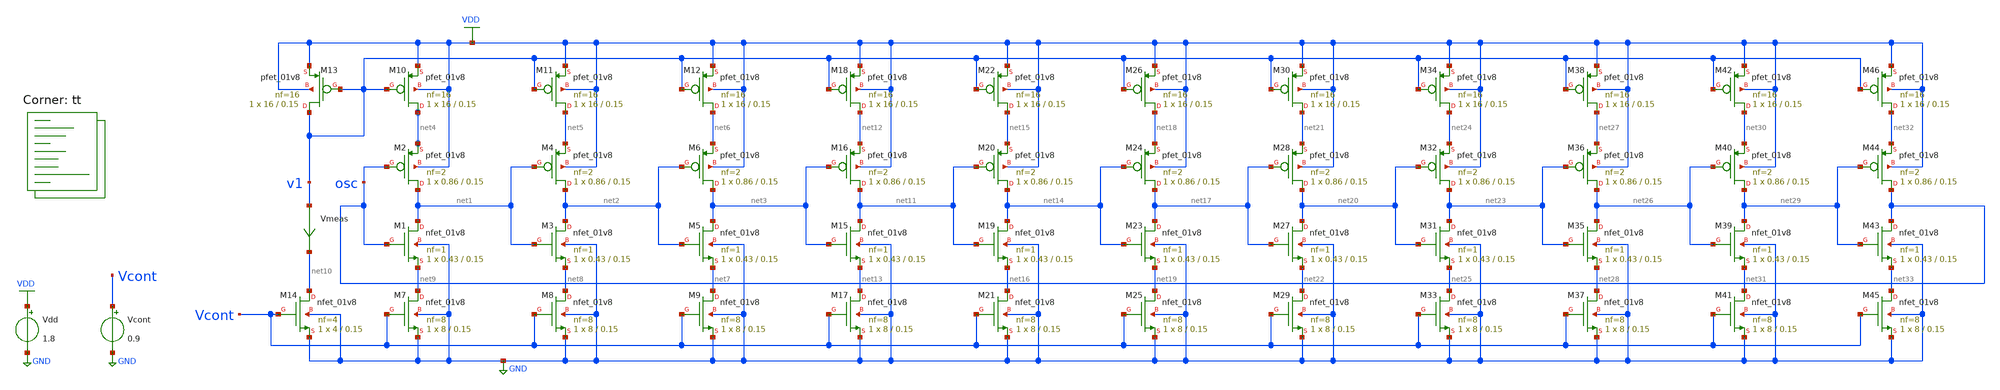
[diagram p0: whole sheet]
** sch_path: projects/pll/vco/xschem_ngspice/tb_current_starved_VCO7.sch
**.subckt tb_current_starved_VCO7
XM1 net1 osc net9 GND sky130_fd_pr__nfet_01v8 L=0.15 W=0.43 nf=1 ad='int((nf+1)/2) * W/nf * 0.29' as='int((nf+2)/2) * W/nf * 0.29'
+ pd='2*int((nf+1)/2) * (W/nf + 0.29)' ps='2*int((nf+2)/2) * (W/nf + 0.29)' nrd='0.29 / W' nrs='0.29 / W'
+ sa=0 sb=0 sd=0 mult=1 m=1
XM2 net1 osc net4 VDD sky130_fd_pr__pfet_01v8 L=0.15 W=0.86 nf=2 ad='int((nf+1)/2) * W/nf * 0.29' as='int((nf+2)/2) * W/nf * 0.29'
+ pd='2*int((nf+1)/2) * (W/nf + 0.29)' ps='2*int((nf+2)/2) * (W/nf + 0.29)' nrd='0.29 / W' nrs='0.29 / W'
+ sa=0 sb=0 sd=0 mult=1 m=1
XM3 net2 net1 net8 GND sky130_fd_pr__nfet_01v8 L=0.15 W=0.43 nf=1 ad='int((nf+1)/2) * W/nf * 0.29' as='int((nf+2)/2) * W/nf * 0.29'
+ pd='2*int((nf+1)/2) * (W/nf + 0.29)' ps='2*int((nf+2)/2) * (W/nf + 0.29)' nrd='0.29 / W' nrs='0.29 / W'
+ sa=0 sb=0 sd=0 mult=1 m=1
XM4 net2 net1 net5 VDD sky130_fd_pr__pfet_01v8 L=0.15 W=0.86 nf=2 ad='int((nf+1)/2) * W/nf * 0.29' as='int((nf+2)/2) * W/nf * 0.29'
+ pd='2*int((nf+1)/2) * (W/nf + 0.29)' ps='2*int((nf+2)/2) * (W/nf + 0.29)' nrd='0.29 / W' nrs='0.29 / W'
+ sa=0 sb=0 sd=0 mult=1 m=1
XM5 net3 net2 net7 GND sky130_fd_pr__nfet_01v8 L=0.15 W=0.43 nf=1 ad='int((nf+1)/2) * W/nf * 0.29' as='int((nf+2)/2) * W/nf * 0.29'
+ pd='2*int((nf+1)/2) * (W/nf + 0.29)' ps='2*int((nf+2)/2) * (W/nf + 0.29)' nrd='0.29 / W' nrs='0.29 / W'
+ sa=0 sb=0 sd=0 mult=1 m=1
XM6 net3 net2 net6 VDD sky130_fd_pr__pfet_01v8 L=0.15 W=0.86 nf=2 ad='int((nf+1)/2) * W/nf * 0.29' as='int((nf+2)/2) * W/nf * 0.29'
+ pd='2*int((nf+1)/2) * (W/nf + 0.29)' ps='2*int((nf+2)/2) * (W/nf + 0.29)' nrd='0.29 / W' nrs='0.29 / W'
+ sa=0 sb=0 sd=0 mult=1 m=1
XM7 net9 Vcont GND GND sky130_fd_pr__nfet_01v8 L=0.15 W=8 nf=8 ad='int((nf+1)/2) * W/nf * 0.29' as='int((nf+2)/2) * W/nf * 0.29'
+ pd='2*int((nf+1)/2) * (W/nf + 0.29)' ps='2*int((nf+2)/2) * (W/nf + 0.29)' nrd='0.29 / W' nrs='0.29 / W'
+ sa=0 sb=0 sd=0 mult=1 m=1
XM8 net8 Vcont GND GND sky130_fd_pr__nfet_01v8 L=0.15 W=8 nf=8 ad='int((nf+1)/2) * W/nf * 0.29' as='int((nf+2)/2) * W/nf * 0.29'
+ pd='2*int((nf+1)/2) * (W/nf + 0.29)' ps='2*int((nf+2)/2) * (W/nf + 0.29)' nrd='0.29 / W' nrs='0.29 / W'
+ sa=0 sb=0 sd=0 mult=1 m=1
XM9 net7 Vcont GND GND sky130_fd_pr__nfet_01v8 L=0.15 W=8 nf=8 ad='int((nf+1)/2) * W/nf * 0.29' as='int((nf+2)/2) * W/nf * 0.29'
+ pd='2*int((nf+1)/2) * (W/nf + 0.29)' ps='2*int((nf+2)/2) * (W/nf + 0.29)' nrd='0.29 / W' nrs='0.29 / W'
+ sa=0 sb=0 sd=0 mult=1 m=1
XM10 net4 v1 VDD VDD sky130_fd_pr__pfet_01v8 L=0.15 W=16 nf=16 ad='int((nf+1)/2) * W/nf * 0.29' as='int((nf+2)/2) * W/nf * 0.29'
+ pd='2*int((nf+1)/2) * (W/nf + 0.29)' ps='2*int((nf+2)/2) * (W/nf + 0.29)' nrd='0.29 / W' nrs='0.29 / W'
+ sa=0 sb=0 sd=0 mult=1 m=1
XM11 net5 v1 VDD VDD sky130_fd_pr__pfet_01v8 L=0.15 W=16 nf=16 ad='int((nf+1)/2) * W/nf * 0.29' as='int((nf+2)/2) * W/nf * 0.29'
+ pd='2*int((nf+1)/2) * (W/nf + 0.29)' ps='2*int((nf+2)/2) * (W/nf + 0.29)' nrd='0.29 / W' nrs='0.29 / W'
+ sa=0 sb=0 sd=0 mult=1 m=1
XM12 net6 v1 VDD VDD sky130_fd_pr__pfet_01v8 L=0.15 W=16 nf=16 ad='int((nf+1)/2) * W/nf * 0.29' as='int((nf+2)/2) * W/nf * 0.29'
+ pd='2*int((nf+1)/2) * (W/nf + 0.29)' ps='2*int((nf+2)/2) * (W/nf + 0.29)' nrd='0.29 / W' nrs='0.29 / W'
+ sa=0 sb=0 sd=0 mult=1 m=1
Vdd VDD GND 1.8
Vcont Vcont GND 0.9
XM13 v1 v1 VDD VDD sky130_fd_pr__pfet_01v8 L=0.15 W=16 nf=16 ad='int((nf+1)/2) * W/nf * 0.29' as='int((nf+2)/2) * W/nf * 0.29'
+ pd='2*int((nf+1)/2) * (W/nf + 0.29)' ps='2*int((nf+2)/2) * (W/nf + 0.29)' nrd='0.29 / W' nrs='0.29 / W'
+ sa=0 sb=0 sd=0 mult=1 m=1
XM14 net10 Vcont GND GND sky130_fd_pr__nfet_01v8 L=0.15 W=4 nf=4 ad='int((nf+1)/2) * W/nf * 0.29' as='int((nf+2)/2) * W/nf * 0.29'
+ pd='2*int((nf+1)/2) * (W/nf + 0.29)' ps='2*int((nf+2)/2) * (W/nf + 0.29)' nrd='0.29 / W' nrs='0.29 / W'
+ sa=0 sb=0 sd=0 mult=1 m=1
Vmeas v1 net10 0
.save i(vmeas)
XM15 net11 net3 net13 GND sky130_fd_pr__nfet_01v8 L=0.15 W=0.43 nf=1 ad='int((nf+1)/2) * W/nf * 0.29'
+ as='int((nf+2)/2) * W/nf * 0.29' pd='2*int((nf+1)/2) * (W/nf + 0.29)' ps='2*int((nf+2)/2) * (W/nf + 0.29)'
+ nrd='0.29 / W' nrs='0.29 / W' sa=0 sb=0 sd=0 mult=1 m=1
XM16 net11 net3 net12 VDD sky130_fd_pr__pfet_01v8 L=0.15 W=0.86 nf=2 ad='int((nf+1)/2) * W/nf * 0.29'
+ as='int((nf+2)/2) * W/nf * 0.29' pd='2*int((nf+1)/2) * (W/nf + 0.29)' ps='2*int((nf+2)/2) * (W/nf + 0.29)'
+ nrd='0.29 / W' nrs='0.29 / W' sa=0 sb=0 sd=0 mult=1 m=1
XM17 net13 Vcont GND GND sky130_fd_pr__nfet_01v8 L=0.15 W=8 nf=8 ad='int((nf+1)/2) * W/nf * 0.29' as='int((nf+2)/2) * W/nf * 0.29'
+ pd='2*int((nf+1)/2) * (W/nf + 0.29)' ps='2*int((nf+2)/2) * (W/nf + 0.29)' nrd='0.29 / W' nrs='0.29 / W'
+ sa=0 sb=0 sd=0 mult=1 m=1
XM18 net12 v1 VDD VDD sky130_fd_pr__pfet_01v8 L=0.15 W=16 nf=16 ad='int((nf+1)/2) * W/nf * 0.29' as='int((nf+2)/2) * W/nf * 0.29'
+ pd='2*int((nf+1)/2) * (W/nf + 0.29)' ps='2*int((nf+2)/2) * (W/nf + 0.29)' nrd='0.29 / W' nrs='0.29 / W'
+ sa=0 sb=0 sd=0 mult=1 m=1
XM19 net14 net11 net16 GND sky130_fd_pr__nfet_01v8 L=0.15 W=0.43 nf=1 ad='int((nf+1)/2) * W/nf * 0.29'
+ as='int((nf+2)/2) * W/nf * 0.29' pd='2*int((nf+1)/2) * (W/nf + 0.29)' ps='2*int((nf+2)/2) * (W/nf + 0.29)'
+ nrd='0.29 / W' nrs='0.29 / W' sa=0 sb=0 sd=0 mult=1 m=1
XM20 net14 net11 net15 VDD sky130_fd_pr__pfet_01v8 L=0.15 W=0.86 nf=2 ad='int((nf+1)/2) * W/nf * 0.29'
+ as='int((nf+2)/2) * W/nf * 0.29' pd='2*int((nf+1)/2) * (W/nf + 0.29)' ps='2*int((nf+2)/2) * (W/nf + 0.29)'
+ nrd='0.29 / W' nrs='0.29 / W' sa=0 sb=0 sd=0 mult=1 m=1
XM21 net16 Vcont GND GND sky130_fd_pr__nfet_01v8 L=0.15 W=8 nf=8 ad='int((nf+1)/2) * W/nf * 0.29' as='int((nf+2)/2) * W/nf * 0.29'
+ pd='2*int((nf+1)/2) * (W/nf + 0.29)' ps='2*int((nf+2)/2) * (W/nf + 0.29)' nrd='0.29 / W' nrs='0.29 / W'
+ sa=0 sb=0 sd=0 mult=1 m=1
XM22 net15 v1 VDD VDD sky130_fd_pr__pfet_01v8 L=0.15 W=16 nf=16 ad='int((nf+1)/2) * W/nf * 0.29' as='int((nf+2)/2) * W/nf * 0.29'
+ pd='2*int((nf+1)/2) * (W/nf + 0.29)' ps='2*int((nf+2)/2) * (W/nf + 0.29)' nrd='0.29 / W' nrs='0.29 / W'
+ sa=0 sb=0 sd=0 mult=1 m=1
XM23 net17 net14 net19 GND sky130_fd_pr__nfet_01v8 L=0.15 W=0.43 nf=1 ad='int((nf+1)/2) * W/nf * 0.29'
+ as='int((nf+2)/2) * W/nf * 0.29' pd='2*int((nf+1)/2) * (W/nf + 0.29)' ps='2*int((nf+2)/2) * (W/nf + 0.29)'
+ nrd='0.29 / W' nrs='0.29 / W' sa=0 sb=0 sd=0 mult=1 m=1
XM24 net17 net14 net18 VDD sky130_fd_pr__pfet_01v8 L=0.15 W=0.86 nf=2 ad='int((nf+1)/2) * W/nf * 0.29'
+ as='int((nf+2)/2) * W/nf * 0.29' pd='2*int((nf+1)/2) * (W/nf + 0.29)' ps='2*int((nf+2)/2) * (W/nf + 0.29)'
+ nrd='0.29 / W' nrs='0.29 / W' sa=0 sb=0 sd=0 mult=1 m=1
XM25 net19 Vcont GND GND sky130_fd_pr__nfet_01v8 L=0.15 W=8 nf=8 ad='int((nf+1)/2) * W/nf * 0.29' as='int((nf+2)/2) * W/nf * 0.29'
+ pd='2*int((nf+1)/2) * (W/nf + 0.29)' ps='2*int((nf+2)/2) * (W/nf + 0.29)' nrd='0.29 / W' nrs='0.29 / W'
+ sa=0 sb=0 sd=0 mult=1 m=1
XM26 net18 v1 VDD VDD sky130_fd_pr__pfet_01v8 L=0.15 W=16 nf=16 ad='int((nf+1)/2) * W/nf * 0.29' as='int((nf+2)/2) * W/nf * 0.29'
+ pd='2*int((nf+1)/2) * (W/nf + 0.29)' ps='2*int((nf+2)/2) * (W/nf + 0.29)' nrd='0.29 / W' nrs='0.29 / W'
+ sa=0 sb=0 sd=0 mult=1 m=1
XM27 net20 net17 net22 GND sky130_fd_pr__nfet_01v8 L=0.15 W=0.43 nf=1 ad='int((nf+1)/2) * W/nf * 0.29'
+ as='int((nf+2)/2) * W/nf * 0.29' pd='2*int((nf+1)/2) * (W/nf + 0.29)' ps='2*int((nf+2)/2) * (W/nf + 0.29)'
+ nrd='0.29 / W' nrs='0.29 / W' sa=0 sb=0 sd=0 mult=1 m=1
XM28 net20 net17 net21 VDD sky130_fd_pr__pfet_01v8 L=0.15 W=0.86 nf=2 ad='int((nf+1)/2) * W/nf * 0.29'
+ as='int((nf+2)/2) * W/nf * 0.29' pd='2*int((nf+1)/2) * (W/nf + 0.29)' ps='2*int((nf+2)/2) * (W/nf + 0.29)'
+ nrd='0.29 / W' nrs='0.29 / W' sa=0 sb=0 sd=0 mult=1 m=1
XM29 net22 Vcont GND GND sky130_fd_pr__nfet_01v8 L=0.15 W=8 nf=8 ad='int((nf+1)/2) * W/nf * 0.29' as='int((nf+2)/2) * W/nf * 0.29'
+ pd='2*int((nf+1)/2) * (W/nf + 0.29)' ps='2*int((nf+2)/2) * (W/nf + 0.29)' nrd='0.29 / W' nrs='0.29 / W'
+ sa=0 sb=0 sd=0 mult=1 m=1
XM30 net21 v1 VDD VDD sky130_fd_pr__pfet_01v8 L=0.15 W=16 nf=16 ad='int((nf+1)/2) * W/nf * 0.29' as='int((nf+2)/2) * W/nf * 0.29'
+ pd='2*int((nf+1)/2) * (W/nf + 0.29)' ps='2*int((nf+2)/2) * (W/nf + 0.29)' nrd='0.29 / W' nrs='0.29 / W'
+ sa=0 sb=0 sd=0 mult=1 m=1
XM31 net23 net20 net25 GND sky130_fd_pr__nfet_01v8 L=0.15 W=0.43 nf=1 ad='int((nf+1)/2) * W/nf * 0.29'
+ as='int((nf+2)/2) * W/nf * 0.29' pd='2*int((nf+1)/2) * (W/nf + 0.29)' ps='2*int((nf+2)/2) * (W/nf + 0.29)'
+ nrd='0.29 / W' nrs='0.29 / W' sa=0 sb=0 sd=0 mult=1 m=1
XM32 net23 net20 net24 VDD sky130_fd_pr__pfet_01v8 L=0.15 W=0.86 nf=2 ad='int((nf+1)/2) * W/nf * 0.29'
+ as='int((nf+2)/2) * W/nf * 0.29' pd='2*int((nf+1)/2) * (W/nf + 0.29)' ps='2*int((nf+2)/2) * (W/nf + 0.29)'
+ nrd='0.29 / W' nrs='0.29 / W' sa=0 sb=0 sd=0 mult=1 m=1
XM33 net25 Vcont GND GND sky130_fd_pr__nfet_01v8 L=0.15 W=8 nf=8 ad='int((nf+1)/2) * W/nf * 0.29' as='int((nf+2)/2) * W/nf * 0.29'
+ pd='2*int((nf+1)/2) * (W/nf + 0.29)' ps='2*int((nf+2)/2) * (W/nf + 0.29)' nrd='0.29 / W' nrs='0.29 / W'
+ sa=0 sb=0 sd=0 mult=1 m=1
XM34 net24 v1 VDD VDD sky130_fd_pr__pfet_01v8 L=0.15 W=16 nf=16 ad='int((nf+1)/2) * W/nf * 0.29' as='int((nf+2)/2) * W/nf * 0.29'
+ pd='2*int((nf+1)/2) * (W/nf + 0.29)' ps='2*int((nf+2)/2) * (W/nf + 0.29)' nrd='0.29 / W' nrs='0.29 / W'
+ sa=0 sb=0 sd=0 mult=1 m=1
XM35 net26 net23 net28 GND sky130_fd_pr__nfet_01v8 L=0.15 W=0.43 nf=1 ad='int((nf+1)/2) * W/nf * 0.29'
+ as='int((nf+2)/2) * W/nf * 0.29' pd='2*int((nf+1)/2) * (W/nf + 0.29)' ps='2*int((nf+2)/2) * (W/nf + 0.29)'
+ nrd='0.29 / W' nrs='0.29 / W' sa=0 sb=0 sd=0 mult=1 m=1
XM36 net26 net23 net27 VDD sky130_fd_pr__pfet_01v8 L=0.15 W=0.86 nf=2 ad='int((nf+1)/2) * W/nf * 0.29'
+ as='int((nf+2)/2) * W/nf * 0.29' pd='2*int((nf+1)/2) * (W/nf + 0.29)' ps='2*int((nf+2)/2) * (W/nf + 0.29)'
+ nrd='0.29 / W' nrs='0.29 / W' sa=0 sb=0 sd=0 mult=1 m=1
XM37 net28 Vcont GND GND sky130_fd_pr__nfet_01v8 L=0.15 W=8 nf=8 ad='int((nf+1)/2) * W/nf * 0.29' as='int((nf+2)/2) * W/nf * 0.29'
+ pd='2*int((nf+1)/2) * (W/nf + 0.29)' ps='2*int((nf+2)/2) * (W/nf + 0.29)' nrd='0.29 / W' nrs='0.29 / W'
+ sa=0 sb=0 sd=0 mult=1 m=1
XM38 net27 v1 VDD VDD sky130_fd_pr__pfet_01v8 L=0.15 W=16 nf=16 ad='int((nf+1)/2) * W/nf * 0.29' as='int((nf+2)/2) * W/nf * 0.29'
+ pd='2*int((nf+1)/2) * (W/nf + 0.29)' ps='2*int((nf+2)/2) * (W/nf + 0.29)' nrd='0.29 / W' nrs='0.29 / W'
+ sa=0 sb=0 sd=0 mult=1 m=1
XM39 net29 net26 net31 GND sky130_fd_pr__nfet_01v8 L=0.15 W=0.43 nf=1 ad='int((nf+1)/2) * W/nf * 0.29'
+ as='int((nf+2)/2) * W/nf * 0.29' pd='2*int((nf+1)/2) * (W/nf + 0.29)' ps='2*int((nf+2)/2) * (W/nf + 0.29)'
+ nrd='0.29 / W' nrs='0.29 / W' sa=0 sb=0 sd=0 mult=1 m=1
XM40 net29 net26 net30 VDD sky130_fd_pr__pfet_01v8 L=0.15 W=0.86 nf=2 ad='int((nf+1)/2) * W/nf * 0.29'
+ as='int((nf+2)/2) * W/nf * 0.29' pd='2*int((nf+1)/2) * (W/nf + 0.29)' ps='2*int((nf+2)/2) * (W/nf + 0.29)'
+ nrd='0.29 / W' nrs='0.29 / W' sa=0 sb=0 sd=0 mult=1 m=1
XM41 net31 Vcont GND GND sky130_fd_pr__nfet_01v8 L=0.15 W=8 nf=8 ad='int((nf+1)/2) * W/nf * 0.29' as='int((nf+2)/2) * W/nf * 0.29'
+ pd='2*int((nf+1)/2) * (W/nf + 0.29)' ps='2*int((nf+2)/2) * (W/nf + 0.29)' nrd='0.29 / W' nrs='0.29 / W'
+ sa=0 sb=0 sd=0 mult=1 m=1
XM42 net30 v1 VDD VDD sky130_fd_pr__pfet_01v8 L=0.15 W=16 nf=16 ad='int((nf+1)/2) * W/nf * 0.29' as='int((nf+2)/2) * W/nf * 0.29'
+ pd='2*int((nf+1)/2) * (W/nf + 0.29)' ps='2*int((nf+2)/2) * (W/nf + 0.29)' nrd='0.29 / W' nrs='0.29 / W'
+ sa=0 sb=0 sd=0 mult=1 m=1
XM43 osc net29 net33 GND sky130_fd_pr__nfet_01v8 L=0.15 W=0.43 nf=1 ad='int((nf+1)/2) * W/nf * 0.29'
+ as='int((nf+2)/2) * W/nf * 0.29' pd='2*int((nf+1)/2) * (W/nf + 0.29)' ps='2*int((nf+2)/2) * (W/nf + 0.29)'
+ nrd='0.29 / W' nrs='0.29 / W' sa=0 sb=0 sd=0 mult=1 m=1
XM44 osc net29 net32 VDD sky130_fd_pr__pfet_01v8 L=0.15 W=0.86 nf=2 ad='int((nf+1)/2) * W/nf * 0.29'
+ as='int((nf+2)/2) * W/nf * 0.29' pd='2*int((nf+1)/2) * (W/nf + 0.29)' ps='2*int((nf+2)/2) * (W/nf + 0.29)'
+ nrd='0.29 / W' nrs='0.29 / W' sa=0 sb=0 sd=0 mult=1 m=1
XM45 net33 Vcont GND GND sky130_fd_pr__nfet_01v8 L=0.15 W=8 nf=8 ad='int((nf+1)/2) * W/nf * 0.29' as='int((nf+2)/2) * W/nf * 0.29'
+ pd='2*int((nf+1)/2) * (W/nf + 0.29)' ps='2*int((nf+2)/2) * (W/nf + 0.29)' nrd='0.29 / W' nrs='0.29 / W'
+ sa=0 sb=0 sd=0 mult=1 m=1
XM46 net32 v1 VDD VDD sky130_fd_pr__pfet_01v8 L=0.15 W=16 nf=16 ad='int((nf+1)/2) * W/nf * 0.29' as='int((nf+2)/2) * W/nf * 0.29'
+ pd='2*int((nf+1)/2) * (W/nf + 0.29)' ps='2*int((nf+2)/2) * (W/nf + 0.29)' nrd='0.29 / W' nrs='0.29 / W'
+ sa=0 sb=0 sd=0 mult=1 m=1
**** begin user architecture code
.lib $::SKYWATER_MODELS/sky130.lib.spice tt



.option method=gear
.option wnflag=1


*.ic v(osc)=0

*.temp = 75

.control
  *let v_cont_start = 0.0
  *let v_cont_stop = 1.9

  *dowhile v_cont_start <= v_cont_stop
    *alter vcont $&v_cont_start
    save v(osc) v(vcont) v(v1)
    linearize v(osc)
    tran 1ps 30ns
    remzerovec
    *write tb_current_starved_VCO7_{$&v_cont_start}.raw
    write tb_current_starved_VCO7.raw
    *let filename = v_cont_start * 100
    *wrdata /foss/designs/my_design/projects/pll/vco/xschem_ngspice/tb_current_starved_VCO7_{$&filename}.txt
+ v(osc)
    wrdata /foss/designs/my_design/projects/pll/vco/xschem_ngspice/tb_current_starved_VCO7.txt
+ v(osc)
    set appendwrite

    *reset
    *let v_cont_start = v_cont_start + 0.1
  *end
.endc






**** end user architecture code
**.ends
.GLOBAL VDD
.GLOBAL GND
.end
